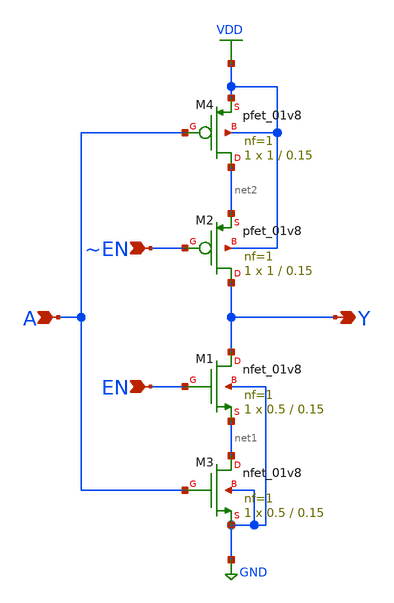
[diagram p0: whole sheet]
** sch_path: library/xschem/tristate.sch
**.subckt tristate A Y EN ~EN
*.ipin A
*.opin Y
*.ipin EN
*.ipin ~EN
XM1 Y EN net1 GND sky130_fd_pr__nfet_01v8 L=0.15 W=0.5 nf=1 ad='int((nf+1)/2) * W/nf * 0.29' as='int((nf+2)/2) * W/nf * 0.29'
+ pd='2*int((nf+1)/2) * (W/nf + 0.29)' ps='2*int((nf+2)/2) * (W/nf + 0.29)' nrd='0.29 / W' nrs='0.29 / W'
+ sa=0 sb=0 sd=0 mult=1 m=1
XM2 Y ~EN net2 VDD sky130_fd_pr__pfet_01v8 L=0.15 W=1 nf=1 ad='int((nf+1)/2) * W/nf * 0.29' as='int((nf+2)/2) * W/nf * 0.29'
+ pd='2*int((nf+1)/2) * (W/nf + 0.29)' ps='2*int((nf+2)/2) * (W/nf + 0.29)' nrd='0.29 / W' nrs='0.29 / W'
+ sa=0 sb=0 sd=0 mult=1 m=1
XM3 net1 A GND GND sky130_fd_pr__nfet_01v8 L=0.15 W=0.5 nf=1 ad='int((nf+1)/2) * W/nf * 0.29' as='int((nf+2)/2) * W/nf * 0.29'
+ pd='2*int((nf+1)/2) * (W/nf + 0.29)' ps='2*int((nf+2)/2) * (W/nf + 0.29)' nrd='0.29 / W' nrs='0.29 / W'
+ sa=0 sb=0 sd=0 mult=1 m=1
XM4 net2 A VDD VDD sky130_fd_pr__pfet_01v8 L=0.15 W=1 nf=1 ad='int((nf+1)/2) * W/nf * 0.29' as='int((nf+2)/2) * W/nf * 0.29'
+ pd='2*int((nf+1)/2) * (W/nf + 0.29)' ps='2*int((nf+2)/2) * (W/nf + 0.29)' nrd='0.29 / W' nrs='0.29 / W'
+ sa=0 sb=0 sd=0 mult=1 m=1
**.ends
.GLOBAL VDD
.GLOBAL GND
.end
